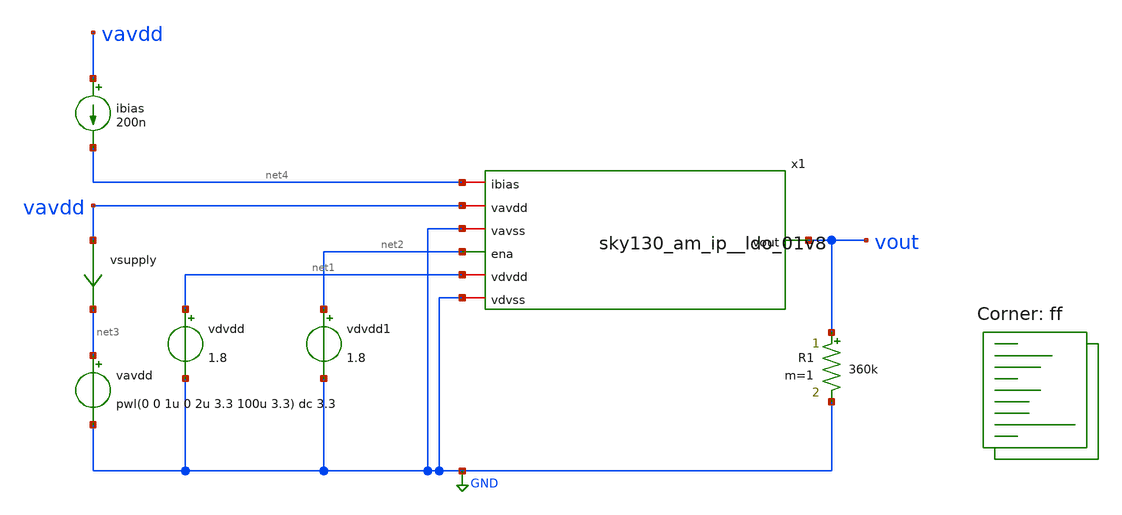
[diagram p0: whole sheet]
** sch_path: xschem/sky130_am_ip__ldo_01v8_tb.sch
**.subckt sky130_am_ip__ldo_01v8_tb
vavdd net3 GND pwl(0 0 1u 0 2u 3.3 100u 3.3) dc 3.3
ibias vavdd net4 200n
vdvdd net1 GND 1.8
vdvdd1 net2 GND 1.8
vsupply vavdd net3 0
.save i(vsupply)
x1 net1 vavdd net4 net2 GND GND vout sky130_am_ip__ldo_01v8
R1 vout GND 360k m=1
**** begin user architecture code

.option savecurrents
.control
save all
op
write sky130_am_ip__ldo_01v8_tb.raw
set appendwrite
quit
.endc


.lib $::SKYWATER_MODELS/sky130.lib.spice ff
**** end user architecture code
**.ends

* expanding   symbol:  sky130_am_ip__ldo_01v8.sym # of pins=7
** sym_path: xschem/sky130_am_ip__ldo_01v8.sym
** sch_path: xschem/sky130_am_ip__ldo_01v8.sch
.subckt sky130_am_ip__ldo_01v8 vdvdd vavdd ibias ena vdvss vavss vout
*.opin vout
*.iopin vavdd
*.iopin vavss
*.ipin ena
*.iopin vdvdd
*.iopin vdvss
*.iopin ibias
XM1 net12 vbn vavss vavss sky130_fd_pr__nfet_g5v0d10v5 L=20 W=1 nf=1 ad='int((nf+1)/2) * W/nf * 0.29'
+ as='int((nf+2)/2) * W/nf * 0.29' pd='2*int((nf+1)/2) * (W/nf + 0.29)' ps='2*int((nf+2)/2) * (W/nf + 0.29)'
+ nrd='0.29 / W' nrs='0.29 / W' sa=0 sb=0 sd=0 mult=5 m=5
XM3 net13 vbn vavss vavss sky130_fd_pr__nfet_g5v0d10v5 L=20 W=1 nf=1 ad='int((nf+1)/2) * W/nf * 0.29'
+ as='int((nf+2)/2) * W/nf * 0.29' pd='2*int((nf+1)/2) * (W/nf + 0.29)' ps='2*int((nf+2)/2) * (W/nf + 0.29)'
+ nrd='0.29 / W' nrs='0.29 / W' sa=0 sb=0 sd=0 mult=5 m=5
XM5 net15 vbp vavdd vavdd sky130_fd_pr__pfet_g5v0d10v5 L=20 W=1 nf=1 ad='int((nf+1)/2) * W/nf * 0.29'
+ as='int((nf+2)/2) * W/nf * 0.29' pd='2*int((nf+1)/2) * (W/nf + 0.29)' ps='2*int((nf+2)/2) * (W/nf + 0.29)'
+ nrd='0.29 / W' nrs='0.29 / W' sa=0 sb=0 sd=0 mult=5 m=5
XM16 net1 net2 vavss vavss sky130_fd_pr__nfet_g5v0d10v5 L=0.5 W=1 nf=1 ad='int((nf+1)/2) * W/nf * 0.29'
+ as='int((nf+2)/2) * W/nf * 0.29' pd='2*int((nf+1)/2) * (W/nf + 0.29)' ps='2*int((nf+2)/2) * (W/nf + 0.29)'
+ nrd='0.29 / W' nrs='0.29 / W' sa=0 sb=0 sd=0 mult=1 m=1
XM17 net2 net2 net1 vavss sky130_fd_pr__nfet_g5v0d10v5 L=0.5 W=1 nf=1 ad='int((nf+1)/2) * W/nf * 0.29'
+ as='int((nf+2)/2) * W/nf * 0.29' pd='2*int((nf+1)/2) * (W/nf + 0.29)' ps='2*int((nf+2)/2) * (W/nf + 0.29)'
+ nrd='0.29 / W' nrs='0.29 / W' sa=0 sb=0 sd=0 mult=4 m=4
XM18 vcn vcn net1 vavss sky130_fd_pr__nfet_g5v0d10v5 L=2 W=4 nf=1 ad='int((nf+1)/2) * W/nf * 0.29' as='int((nf+2)/2) * W/nf * 0.29'
+ pd='2*int((nf+1)/2) * (W/nf + 0.29)' ps='2*int((nf+2)/2) * (W/nf + 0.29)' nrd='0.29 / W' nrs='0.29 / W'
+ sa=0 sb=0 sd=0 mult=1 m=1
Vmeas vbp net14 0
.save i(vmeas)
Vmeas5 net23 net2 0
.save i(vmeas5)
Vmeas6 net25 vcn 0
.save i(vmeas6)
XM22 net3 vbp vavdd vavdd sky130_fd_pr__pfet_g5v0d10v5 L=20 W=1 nf=1 ad='int((nf+1)/2) * W/nf * 0.29'
+ as='int((nf+2)/2) * W/nf * 0.29' pd='2*int((nf+1)/2) * (W/nf + 0.29)' ps='2*int((nf+2)/2) * (W/nf + 0.29)'
+ nrd='0.29 / W' nrs='0.29 / W' sa=0 sb=0 sd=0 mult=4 m=4
XM23 net4 vcp net3 vavdd sky130_fd_pr__pfet_g5v0d10v5 L=8 W=16 nf=1 ad='int((nf+1)/2) * W/nf * 0.29'
+ as='int((nf+2)/2) * W/nf * 0.29' pd='2*int((nf+1)/2) * (W/nf + 0.29)' ps='2*int((nf+2)/2) * (W/nf + 0.29)'
+ nrd='0.29 / W' nrs='0.29 / W' sa=0 sb=0 sd=0 mult=1 m=1
Vmeas8 net4 net5 0
.save i(vmeas8)
XM24 net7 v_m net5 vavdd sky130_fd_pr__pfet_g5v0d10v5 L=0.5 W=40 nf=1 ad='int((nf+1)/2) * W/nf * 0.29'
+ as='int((nf+2)/2) * W/nf * 0.29' pd='2*int((nf+1)/2) * (W/nf + 0.29)' ps='2*int((nf+2)/2) * (W/nf + 0.29)'
+ nrd='0.29 / W' nrs='0.29 / W' sa=0 sb=0 sd=0 mult=1 m=1
XM25 net6 v_p net5 vavdd sky130_fd_pr__pfet_g5v0d10v5 L=0.5 W=40 nf=1 ad='int((nf+1)/2) * W/nf * 0.29'
+ as='int((nf+2)/2) * W/nf * 0.29' pd='2*int((nf+1)/2) * (W/nf + 0.29)' ps='2*int((nf+2)/2) * (W/nf + 0.29)'
+ nrd='0.29 / W' nrs='0.29 / W' sa=0 sb=0 sd=0 mult=1 m=1
XM26 net9 net8 vavdd vavdd sky130_fd_pr__pfet_g5v0d10v5 L=0.5 W=1 nf=1 ad='int((nf+1)/2) * W/nf * 0.29'
+ as='int((nf+2)/2) * W/nf * 0.29' pd='2*int((nf+1)/2) * (W/nf + 0.29)' ps='2*int((nf+2)/2) * (W/nf + 0.29)'
+ nrd='0.29 / W' nrs='0.29 / W' sa=0 sb=0 sd=0 mult=1 m=1
XM27 net10 net8 vavdd vavdd sky130_fd_pr__pfet_g5v0d10v5 L=0.5 W=1 nf=1 ad='int((nf+1)/2) * W/nf * 0.29'
+ as='int((nf+2)/2) * W/nf * 0.29' pd='2*int((nf+1)/2) * (W/nf + 0.29)' ps='2*int((nf+2)/2) * (W/nf + 0.29)'
+ nrd='0.29 / W' nrs='0.29 / W' sa=0 sb=0 sd=0 mult=1 m=1
XM28 net8 vcp net9 vavdd sky130_fd_pr__pfet_g5v0d10v5 L=0.5 W=1 nf=1 ad='int((nf+1)/2) * W/nf * 0.29'
+ as='int((nf+2)/2) * W/nf * 0.29' pd='2*int((nf+1)/2) * (W/nf + 0.29)' ps='2*int((nf+2)/2) * (W/nf + 0.29)'
+ nrd='0.29 / W' nrs='0.29 / W' sa=0 sb=0 sd=0 mult=1 m=1
XM29 v_x vcp net10 vavdd sky130_fd_pr__pfet_g5v0d10v5 L=0.5 W=1 nf=1 ad='int((nf+1)/2) * W/nf * 0.29'
+ as='int((nf+2)/2) * W/nf * 0.29' pd='2*int((nf+1)/2) * (W/nf + 0.29)' ps='2*int((nf+2)/2) * (W/nf + 0.29)'
+ nrd='0.29 / W' nrs='0.29 / W' sa=0 sb=0 sd=0 mult=1 m=1
XM30 net11 vcn net6 vavss sky130_fd_pr__nfet_g5v0d10v5 L=0.5 W=1 nf=1 ad='int((nf+1)/2) * W/nf * 0.29'
+ as='int((nf+2)/2) * W/nf * 0.29' pd='2*int((nf+1)/2) * (W/nf + 0.29)' ps='2*int((nf+2)/2) * (W/nf + 0.29)'
+ nrd='0.29 / W' nrs='0.29 / W' sa=0 sb=0 sd=0 mult=1 m=1
XM31 v_x vcn net7 vavss sky130_fd_pr__nfet_g5v0d10v5 L=0.5 W=1 nf=1 ad='int((nf+1)/2) * W/nf * 0.29'
+ as='int((nf+2)/2) * W/nf * 0.29' pd='2*int((nf+1)/2) * (W/nf + 0.29)' ps='2*int((nf+2)/2) * (W/nf + 0.29)'
+ nrd='0.29 / W' nrs='0.29 / W' sa=0 sb=0 sd=0 mult=1 m=1
XM32 net6 vbn vavss vavss sky130_fd_pr__nfet_g5v0d10v5 L=20 W=1 nf=1 ad='int((nf+1)/2) * W/nf * 0.29'
+ as='int((nf+2)/2) * W/nf * 0.29' pd='2*int((nf+1)/2) * (W/nf + 0.29)' ps='2*int((nf+2)/2) * (W/nf + 0.29)'
+ nrd='0.29 / W' nrs='0.29 / W' sa=0 sb=0 sd=0 mult=5 m=5
XM33 net7 vbn vavss vavss sky130_fd_pr__nfet_g5v0d10v5 L=20 W=1 nf=1 ad='int((nf+1)/2) * W/nf * 0.29'
+ as='int((nf+2)/2) * W/nf * 0.29' pd='2*int((nf+1)/2) * (W/nf + 0.29)' ps='2*int((nf+2)/2) * (W/nf + 0.29)'
+ nrd='0.29 / W' nrs='0.29 / W' sa=0 sb=0 sd=0 mult=5 m=5
Vmeas9 net8 net11 0
.save i(vmeas9)
XM2 vbn vcn net12 vavss sky130_fd_pr__nfet_g5v0d10v5 L=2 W=4 nf=1 ad='int((nf+1)/2) * W/nf * 0.29' as='int((nf+2)/2) * W/nf * 0.29'
+ pd='2*int((nf+1)/2) * (W/nf + 0.29)' ps='2*int((nf+2)/2) * (W/nf + 0.29)' nrd='0.29 / W' nrs='0.29 / W'
+ sa=0 sb=0 sd=0 mult=1 m=1
XM4 net14 vcn net13 vavss sky130_fd_pr__nfet_g5v0d10v5 L=2 W=4 nf=1 ad='int((nf+1)/2) * W/nf * 0.29'
+ as='int((nf+2)/2) * W/nf * 0.29' pd='2*int((nf+1)/2) * (W/nf + 0.29)' ps='2*int((nf+2)/2) * (W/nf + 0.29)'
+ nrd='0.29 / W' nrs='0.29 / W' sa=0 sb=0 sd=0 mult=1 m=1
XM34 vbp vcp net15 vavdd sky130_fd_pr__pfet_g5v0d10v5 L=8 W=16 nf=1 ad='int((nf+1)/2) * W/nf * 0.29'
+ as='int((nf+2)/2) * W/nf * 0.29' pd='2*int((nf+1)/2) * (W/nf + 0.29)' ps='2*int((nf+2)/2) * (W/nf + 0.29)'
+ nrd='0.29 / W' nrs='0.29 / W' sa=0 sb=0 sd=0 mult=1 m=1
XM6 net16 net17 vavdd vavdd sky130_fd_pr__pfet_g5v0d10v5 L=0.5 W=1 nf=1 ad='int((nf+1)/2) * W/nf * 0.29'
+ as='int((nf+2)/2) * W/nf * 0.29' pd='2*int((nf+1)/2) * (W/nf + 0.29)' ps='2*int((nf+2)/2) * (W/nf + 0.29)'
+ nrd='0.29 / W' nrs='0.29 / W' sa=0 sb=0 sd=0 mult=1 m=1
XM7 net17 net17 net16 vavdd sky130_fd_pr__pfet_g5v0d10v5 L=0.5 W=1 nf=1 ad='int((nf+1)/2) * W/nf * 0.29'
+ as='int((nf+2)/2) * W/nf * 0.29' pd='2*int((nf+1)/2) * (W/nf + 0.29)' ps='2*int((nf+2)/2) * (W/nf + 0.29)'
+ nrd='0.29 / W' nrs='0.29 / W' sa=0 sb=0 sd=0 mult=4 m=4
Vmeas1 net17 net21 0
.save i(vmeas1)
XM40 vcp vcp net16 vavdd sky130_fd_pr__pfet_g5v0d10v5 L=8 W=16 nf=1 ad='int((nf+1)/2) * W/nf * 0.29'
+ as='int((nf+2)/2) * W/nf * 0.29' pd='2*int((nf+1)/2) * (W/nf + 0.29)' ps='2*int((nf+2)/2) * (W/nf + 0.29)'
+ nrd='0.29 / W' nrs='0.29 / W' sa=0 sb=0 sd=0 mult=1 m=1
Vmeas2 vcp net28 0
.save i(vmeas2)
XM8 v_ea v_x vavdd vavdd sky130_fd_pr__pfet_g5v0d10v5 L=2 W=20 nf=1 ad='int((nf+1)/2) * W/nf * 0.29'
+ as='int((nf+2)/2) * W/nf * 0.29' pd='2*int((nf+1)/2) * (W/nf + 0.29)' ps='2*int((nf+2)/2) * (W/nf + 0.29)'
+ nrd='0.29 / W' nrs='0.29 / W' sa=0 sb=0 sd=0 mult=1 m=1
XM9 v_ea vcn net18 vavss sky130_fd_pr__nfet_g5v0d10v5 L=2 W=4 nf=1 ad='int((nf+1)/2) * W/nf * 0.29' as='int((nf+2)/2) * W/nf * 0.29'
+ pd='2*int((nf+1)/2) * (W/nf + 0.29)' ps='2*int((nf+2)/2) * (W/nf + 0.29)' nrd='0.29 / W' nrs='0.29 / W'
+ sa=0 sb=0 sd=0 mult=1 m=1
XM10 net18 vbn vavss vavss sky130_fd_pr__nfet_g5v0d10v5 L=20 W=1 nf=1 ad='int((nf+1)/2) * W/nf * 0.29'
+ as='int((nf+2)/2) * W/nf * 0.29' pd='2*int((nf+1)/2) * (W/nf + 0.29)' ps='2*int((nf+2)/2) * (W/nf + 0.29)'
+ nrd='0.29 / W' nrs='0.29 / W' sa=0 sb=0 sd=0 mult=5 m=5
XM11 vavdd net26 vout vavss sky130_fd_pr__nfet_g5v0d10v5 L=1 W=200 nf=1 ad='int((nf+1)/2) * W/nf * 0.29'
+ as='int((nf+2)/2) * W/nf * 0.29' pd='2*int((nf+1)/2) * (W/nf + 0.29)' ps='2*int((nf+2)/2) * (W/nf + 0.29)'
+ nrd='0.29 / W' nrs='0.29 / W' sa=0 sb=0 sd=0 mult=1 m=1
C1 v_ea v_x 100e-15 m=1
XM12 net19 vbn vavss vavss sky130_fd_pr__nfet_g5v0d10v5 L=20 W=1 nf=1 ad='int((nf+1)/2) * W/nf * 0.29'
+ as='int((nf+2)/2) * W/nf * 0.29' pd='2*int((nf+1)/2) * (W/nf + 0.29)' ps='2*int((nf+2)/2) * (W/nf + 0.29)'
+ nrd='0.29 / W' nrs='0.29 / W' sa=0 sb=0 sd=0 mult=5 m=5
XM13 net28 vcn net19 vavss sky130_fd_pr__nfet_g5v0d10v5 L=2 W=4 nf=1 ad='int((nf+1)/2) * W/nf * 0.29'
+ as='int((nf+2)/2) * W/nf * 0.29' pd='2*int((nf+1)/2) * (W/nf + 0.29)' ps='2*int((nf+2)/2) * (W/nf + 0.29)'
+ nrd='0.29 / W' nrs='0.29 / W' sa=0 sb=0 sd=0 mult=1 m=1
XM14 net20 vbn vavss vavss sky130_fd_pr__nfet_g5v0d10v5 L=20 W=1 nf=1 ad='int((nf+1)/2) * W/nf * 0.29'
+ as='int((nf+2)/2) * W/nf * 0.29' pd='2*int((nf+1)/2) * (W/nf + 0.29)' ps='2*int((nf+2)/2) * (W/nf + 0.29)'
+ nrd='0.29 / W' nrs='0.29 / W' sa=0 sb=0 sd=0 mult=1 m=1
XM15 net21 vcn net20 vavss sky130_fd_pr__nfet_g5v0d10v5 L=2 W=4 nf=1 ad='int((nf+1)/2) * W/nf * 0.29'
+ as='int((nf+2)/2) * W/nf * 0.29' pd='2*int((nf+1)/2) * (W/nf + 0.29)' ps='2*int((nf+2)/2) * (W/nf + 0.29)'
+ nrd='0.29 / W' nrs='0.29 / W' sa=0 sb=0 sd=0 mult=1 m=1
XM19 net22 vbp vavdd vavdd sky130_fd_pr__pfet_g5v0d10v5 L=20 W=1 nf=1 ad='int((nf+1)/2) * W/nf * 0.29'
+ as='int((nf+2)/2) * W/nf * 0.29' pd='2*int((nf+1)/2) * (W/nf + 0.29)' ps='2*int((nf+2)/2) * (W/nf + 0.29)'
+ nrd='0.29 / W' nrs='0.29 / W' sa=0 sb=0 sd=0 mult=1 m=1
XM20 net23 vcp net22 vavdd sky130_fd_pr__pfet_g5v0d10v5 L=8 W=16 nf=1 ad='int((nf+1)/2) * W/nf * 0.29'
+ as='int((nf+2)/2) * W/nf * 0.29' pd='2*int((nf+1)/2) * (W/nf + 0.29)' ps='2*int((nf+2)/2) * (W/nf + 0.29)'
+ nrd='0.29 / W' nrs='0.29 / W' sa=0 sb=0 sd=0 mult=1 m=1
XM21 net24 vbp vavdd vavdd sky130_fd_pr__pfet_g5v0d10v5 L=20 W=1 nf=1 ad='int((nf+1)/2) * W/nf * 0.29'
+ as='int((nf+2)/2) * W/nf * 0.29' pd='2*int((nf+1)/2) * (W/nf + 0.29)' ps='2*int((nf+2)/2) * (W/nf + 0.29)'
+ nrd='0.29 / W' nrs='0.29 / W' sa=0 sb=0 sd=0 mult=5 m=5
XM35 net25 vcp net24 vavdd sky130_fd_pr__pfet_g5v0d10v5 L=8 W=16 nf=1 ad='int((nf+1)/2) * W/nf * 0.29'
+ as='int((nf+2)/2) * W/nf * 0.29' pd='2*int((nf+1)/2) * (W/nf + 0.29)' ps='2*int((nf+2)/2) * (W/nf + 0.29)'
+ nrd='0.29 / W' nrs='0.29 / W' sa=0 sb=0 sd=0 mult=1 m=1
XM37 v_m v_m vavss vavss sky130_fd_pr__nfet_g5v0d10v5 L=20 W=2.48 nf=1 ad='int((nf+1)/2) * W/nf * 0.29'
+ as='int((nf+2)/2) * W/nf * 0.29' pd='2*int((nf+1)/2) * (W/nf + 0.29)' ps='2*int((nf+2)/2) * (W/nf + 0.29)'
+ nrd='0.29 / W' nrs='0.29 / W' sa=0 sb=0 sd=0 mult=1 m=1
XR1 v_p vout vavss sky130_fd_pr__res_high_po_0p35 L=1000 mult=1 m=1
XR2 vavss v_p vavss sky130_fd_pr__res_high_po_0p35 L=2000 mult=1 m=1
XM38 net26 v_ena_b v_ea vavdd sky130_fd_pr__pfet_g5v0d10v5 L=20 W=1 nf=1 ad='int((nf+1)/2) * W/nf * 0.29'
+ as='int((nf+2)/2) * W/nf * 0.29' pd='2*int((nf+1)/2) * (W/nf + 0.29)' ps='2*int((nf+2)/2) * (W/nf + 0.29)'
+ nrd='0.29 / W' nrs='0.29 / W' sa=0 sb=0 sd=0 mult=1 m=1
XM39 net26 v_ena_b vavss vavss sky130_fd_pr__nfet_g5v0d10v5 L=20 W=2.47 nf=1 ad='int((nf+1)/2) * W/nf * 0.29'
+ as='int((nf+2)/2) * W/nf * 0.29' pd='2*int((nf+1)/2) * (W/nf + 0.29)' ps='2*int((nf+2)/2) * (W/nf + 0.29)'
+ nrd='0.29 / W' nrs='0.29 / W' sa=0 sb=0 sd=0 mult=1 m=1
XM41 ena_b ena vdvdd vdvdd sky130_fd_pr__pfet_g5v0d10v5 L=0.5 W=2.5 nf=1 ad='int((nf+1)/2) * W/nf * 0.29'
+ as='int((nf+2)/2) * W/nf * 0.29' pd='2*int((nf+1)/2) * (W/nf + 0.29)' ps='2*int((nf+2)/2) * (W/nf + 0.29)'
+ nrd='0.29 / W' nrs='0.29 / W' sa=0 sb=0 sd=0 mult=1 m=1
XM42 ena_b ena vdvss vdvss sky130_fd_pr__nfet_g5v0d10v5 L=0.5 W=1 nf=1 ad='int((nf+1)/2) * W/nf * 0.29'
+ as='int((nf+2)/2) * W/nf * 0.29' pd='2*int((nf+1)/2) * (W/nf + 0.29)' ps='2*int((nf+2)/2) * (W/nf + 0.29)'
+ nrd='0.29 / W' nrs='0.29 / W' sa=0 sb=0 sd=0 mult=1 m=1
XM43 v_ena v_ena_b vavdd vavdd sky130_fd_pr__pfet_g5v0d10v5 L=0.5 W=2.5 nf=1 ad='int((nf+1)/2) * W/nf * 0.29'
+ as='int((nf+2)/2) * W/nf * 0.29' pd='2*int((nf+1)/2) * (W/nf + 0.29)' ps='2*int((nf+2)/2) * (W/nf + 0.29)'
+ nrd='0.29 / W' nrs='0.29 / W' sa=0 sb=0 sd=0 mult=1 m=1
XM44 v_ena ena_b vavss vavss sky130_fd_pr__nfet_g5v0d10v5 L=0.5 W=1 nf=1 ad='int((nf+1)/2) * W/nf * 0.29'
+ as='int((nf+2)/2) * W/nf * 0.29' pd='2*int((nf+1)/2) * (W/nf + 0.29)' ps='2*int((nf+2)/2) * (W/nf + 0.29)'
+ nrd='0.29 / W' nrs='0.29 / W' sa=0 sb=0 sd=0 mult=1 m=1
XM45 v_ena_b v_ena vavdd vavdd sky130_fd_pr__pfet_g5v0d10v5 L=0.5 W=2.5 nf=1 ad='int((nf+1)/2) * W/nf * 0.29'
+ as='int((nf+2)/2) * W/nf * 0.29' pd='2*int((nf+1)/2) * (W/nf + 0.29)' ps='2*int((nf+2)/2) * (W/nf + 0.29)'
+ nrd='0.29 / W' nrs='0.29 / W' sa=0 sb=0 sd=0 mult=1 m=1
XM46 v_ena_b ena vavss vavss sky130_fd_pr__nfet_g5v0d10v5 L=0.5 W=1 nf=1 ad='int((nf+1)/2) * W/nf * 0.29'
+ as='int((nf+2)/2) * W/nf * 0.29' pd='2*int((nf+1)/2) * (W/nf + 0.29)' ps='2*int((nf+2)/2) * (W/nf + 0.29)'
+ nrd='0.29 / W' nrs='0.29 / W' sa=0 sb=0 sd=0 mult=1 m=1
XM47 net27 v_ena vbn vavss sky130_fd_pr__nfet_g5v0d10v5 L=0.5 W=10 nf=1 ad='int((nf+1)/2) * W/nf * 0.29'
+ as='int((nf+2)/2) * W/nf * 0.29' pd='2*int((nf+1)/2) * (W/nf + 0.29)' ps='2*int((nf+2)/2) * (W/nf + 0.29)'
+ nrd='0.29 / W' nrs='0.29 / W' sa=0 sb=0 sd=0 mult=1 m=1
Vmeas3 ibias net27 0
.save i(vmeas3)
XM48 v_m v_m net29 vavdd sky130_fd_pr__pfet_g5v0d10v5 L=20 W=1 nf=1 ad='int((nf+1)/2) * W/nf * 0.29'
+ as='int((nf+2)/2) * W/nf * 0.29' pd='2*int((nf+1)/2) * (W/nf + 0.29)' ps='2*int((nf+2)/2) * (W/nf + 0.29)'
+ nrd='0.29 / W' nrs='0.29 / W' sa=0 sb=0 sd=0 mult=1 m=1
Vmeas4 vavdd net29 0
.save i(vmeas4)
.ends

.GLOBAL GND
.end
